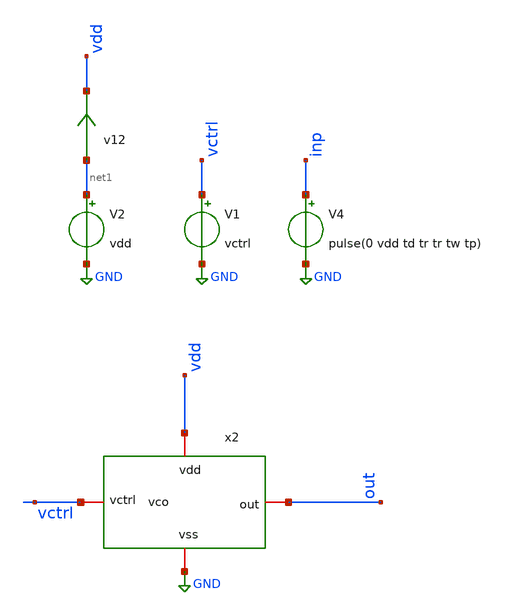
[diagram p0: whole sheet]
** sch_path: xschem/vco/vco_tran.sch
**.subckt vco_tran
V1 vctrl GND vctrl
V2 net1 GND vdd
V4 inp GND pulse(0 vdd td tr tr tw tp)
v12 net1 vdd 0
.save i(v12)
x2 vdd out vctrl GND vco
**** begin user architecture code

** opencircuitdesign pdks install
.lib $::SKYWATER_MODELS/sky130.lib.spice tt
.include $::SKYWATER_STDCELLS/sky130_fd_sc_hd.spice




.options acct list
.temp 25
.save all
.save @m.x2.xm1.msky130_fd_pr__nfet_01v8[cgd]
.save @m.x2.xm4.msky130_fd_pr__pfet_01v8[cgd]
.save @m.x2.xm4.msky130_fd_pr__pfet_01v8[cgg]

.save @m.x2.xm6.msky130_fd_pr__nfet_01v8[cgd]
.save @m.x2.xm6.msky130_fd_pr__nfet_01v8[cgg]

.save @m.x2.xm1.msky130_fd_pr__nfet_01v8[gm]

.save @m.x2.xm2.msky130_fd_pr__pfet_01v8[vth]
.save @m.x2.xm1.msky130_fd_pr__nfet_01v8[vth]
.save @m.x2.xm5.msky130_fd_pr__nfet_01v8[vth]


.param vctrl=0.75 vdd=1.7 cload=250f  td=20n tr=0.1n tw=10n  tp=20n

.control
op
write vco_tran.raw
set appendwrite

tran 0.01n 800n uic
meas tran tdelay01 TRIG v(out) VAL=0.9 RISE=6 TARG v(out) VAL=0.9 RISE=7
let fosc1= 1/tdelay01
print fosc1
save fosc1
remzerovec
write vco_tran.raw
set appendwrite


alterparam vctrl=0.85
reset
tran 0.01n 800n uic
meas tran tdelay01 TRIG v(out) VAL=0.9 RISE=6 TARG v(out) VAL=0.9 RISE=7
let fosc1= 1/tdelay01
print fosc1
save fosc1
remzerovec
write vco_tran.raw
set appendwrite


alterparam vctrl=0.95
reset
tran 0.01n 800n uic
meas tran tdelay01 TRIG v(out) VAL=0.9 RISE=6 TARG v(out) VAL=0.9 RISE=7
let fosc1= 1/tdelay01
print fosc1
save fosc1
remzerovec
write vco_tran.raw
set appendwrite

alterparam vctrl=1.05
reset
tran 0.01n 800n uic
meas tran tdelay01 TRIG v(out) VAL=0.9 RISE=6 TARG v(out) VAL=0.9 RISE=7
let fosc1= 1/tdelay01
print fosc1
save fosc1
remzerovec
write vco_tran.raw
set appendwrite

alterparam vctrl=1.15
reset
tran 0.01n 800n uic
meas tran tdelay01 TRIG v(out) VAL=0.9 RISE=6 TARG v(out) VAL=0.9 RISE=7
let fosc1= 1/tdelay01
print fosc1
save fosc1
remzerovec
write vco_tran.raw
set appendwrite

alterparam vctrl=1.25
reset
tran 0.01n 800n uic
meas tran tdelay01 TRIG v(out) VAL=0.9 RISE=6 TARG v(out) VAL=0.9 RISE=7
let fosc1= 1/tdelay01
print fosc1
save fosc1
remzerovec
write vco_tran.raw
set appendwrite

.endc


**** end user architecture code
**.ends

* expanding   symbol:  vco/vco.sym # of pins=4
** sym_path: xschem01/vco/vco.sym
** sch_path: xschem01/vco/vco.sch
.subckt vco vdd out vctrl vss
*.iopin vdd
*.iopin vss
*.iopin out
*.iopin vctrl
XM1 net1 vctrl vss vss sky130_fd_pr__nfet_01v8 L=0.15 W=30 nf=1 ad='int((nf+1)/2) * W/nf * 0.29' as='int((nf+2)/2) * W/nf * 0.29'
+ pd='2*int((nf+1)/2) * (W/nf + 0.29)' ps='2*int((nf+2)/2) * (W/nf + 0.29)' nrd='0.29 / W' nrs='0.29 / W'
+ sa=0 sb=0 sd=0 mult=1 m=1
XM2 net1 net1 vdd vdd sky130_fd_pr__pfet_01v8 L=0.15 W=90 nf=1 ad='int((nf+1)/2) * W/nf * 0.29' as='int((nf+2)/2) * W/nf * 0.29'
+ pd='2*int((nf+1)/2) * (W/nf + 0.29)' ps='2*int((nf+2)/2) * (W/nf + 0.29)' nrd='0.29 / W' nrs='0.29 / W'
+ sa=0 sb=0 sd=0 mult=1 m=1
XM3 net4 net1 vdd vdd sky130_fd_pr__pfet_01v8 L=0.15 W=80 nf=1 ad='int((nf+1)/2) * W/nf * 0.29' as='int((nf+2)/2) * W/nf * 0.29'
+ pd='2*int((nf+1)/2) * (W/nf + 0.29)' ps='2*int((nf+2)/2) * (W/nf + 0.29)' nrd='0.29 / W' nrs='0.29 / W'
+ sa=0 sb=0 sd=0 mult=1 m=1
XM4 net3 out net4 net4 sky130_fd_pr__pfet_01v8 L=0.15 W=80 nf=1 ad='int((nf+1)/2) * W/nf * 0.29' as='int((nf+2)/2) * W/nf * 0.29'
+ pd='2*int((nf+1)/2) * (W/nf + 0.29)' ps='2*int((nf+2)/2) * (W/nf + 0.29)' nrd='0.29 / W' nrs='0.29 / W'
+ sa=0 sb=0 sd=0 mult=1 m=1
XM5 net2 vctrl vss vss sky130_fd_pr__nfet_01v8 L=0.15 W=30 nf=1 ad='int((nf+1)/2) * W/nf * 0.29' as='int((nf+2)/2) * W/nf * 0.29'
+ pd='2*int((nf+1)/2) * (W/nf + 0.29)' ps='2*int((nf+2)/2) * (W/nf + 0.29)' nrd='0.29 / W' nrs='0.29 / W'
+ sa=0 sb=0 sd=0 mult=1 m=1
XM6 net3 out net2 vss sky130_fd_pr__nfet_01v8 L=0.15 W=30 nf=1 ad='int((nf+1)/2) * W/nf * 0.29' as='int((nf+2)/2) * W/nf * 0.29'
+ pd='2*int((nf+1)/2) * (W/nf + 0.29)' ps='2*int((nf+2)/2) * (W/nf + 0.29)' nrd='0.29 / W' nrs='0.29 / W'
+ sa=0 sb=0 sd=0 mult=1 m=1
XM7 net7 net1 vdd vdd sky130_fd_pr__pfet_01v8 L=0.15 W=80 nf=1 ad='int((nf+1)/2) * W/nf * 0.29' as='int((nf+2)/2) * W/nf * 0.29'
+ pd='2*int((nf+1)/2) * (W/nf + 0.29)' ps='2*int((nf+2)/2) * (W/nf + 0.29)' nrd='0.29 / W' nrs='0.29 / W'
+ sa=0 sb=0 sd=0 mult=2 m=2
XM8 net6 net3 net7 net7 sky130_fd_pr__pfet_01v8 L=0.15 W=80 nf=1 ad='int((nf+1)/2) * W/nf * 0.29' as='int((nf+2)/2) * W/nf * 0.29'
+ pd='2*int((nf+1)/2) * (W/nf + 0.29)' ps='2*int((nf+2)/2) * (W/nf + 0.29)' nrd='0.29 / W' nrs='0.29 / W'
+ sa=0 sb=0 sd=0 mult=2 m=2
XM9 net5 vctrl vss vss sky130_fd_pr__nfet_01v8 L=0.15 W=60 nf=1 ad='int((nf+1)/2) * W/nf * 0.29' as='int((nf+2)/2) * W/nf * 0.29'
+ pd='2*int((nf+1)/2) * (W/nf + 0.29)' ps='2*int((nf+2)/2) * (W/nf + 0.29)' nrd='0.29 / W' nrs='0.29 / W'
+ sa=0 sb=0 sd=0 mult=1 m=1
XM10 net6 net3 net5 vss sky130_fd_pr__nfet_01v8 L=0.15 W=60 nf=1 ad='int((nf+1)/2) * W/nf * 0.29' as='int((nf+2)/2) * W/nf * 0.29'
+ pd='2*int((nf+1)/2) * (W/nf + 0.29)' ps='2*int((nf+2)/2) * (W/nf + 0.29)' nrd='0.29 / W' nrs='0.29 / W'
+ sa=0 sb=0 sd=0 mult=1 m=1
XM11 net9 net1 vdd vdd sky130_fd_pr__pfet_01v8 L=0.15 W=80 nf=1 ad='int((nf+1)/2) * W/nf * 0.29' as='int((nf+2)/2) * W/nf * 0.29'
+ pd='2*int((nf+1)/2) * (W/nf + 0.29)' ps='2*int((nf+2)/2) * (W/nf + 0.29)' nrd='0.29 / W' nrs='0.29 / W'
+ sa=0 sb=0 sd=0 mult=3 m=3
XM12 out net6 net9 net9 sky130_fd_pr__pfet_01v8 L=0.15 W=80 nf=1 ad='int((nf+1)/2) * W/nf * 0.29' as='int((nf+2)/2) * W/nf * 0.29'
+ pd='2*int((nf+1)/2) * (W/nf + 0.29)' ps='2*int((nf+2)/2) * (W/nf + 0.29)' nrd='0.29 / W' nrs='0.29 / W'
+ sa=0 sb=0 sd=0 mult=3 m=3
XM13 net8 vctrl vss vss sky130_fd_pr__nfet_01v8 L=0.15 W=90 nf=1 ad='int((nf+1)/2) * W/nf * 0.29' as='int((nf+2)/2) * W/nf * 0.29'
+ pd='2*int((nf+1)/2) * (W/nf + 0.29)' ps='2*int((nf+2)/2) * (W/nf + 0.29)' nrd='0.29 / W' nrs='0.29 / W'
+ sa=0 sb=0 sd=0 mult=1 m=1
XM14 out net6 net8 vss sky130_fd_pr__nfet_01v8 L=0.15 W=90 nf=1 ad='int((nf+1)/2) * W/nf * 0.29' as='int((nf+2)/2) * W/nf * 0.29'
+ pd='2*int((nf+1)/2) * (W/nf + 0.29)' ps='2*int((nf+2)/2) * (W/nf + 0.29)' nrd='0.29 / W' nrs='0.29 / W'
+ sa=0 sb=0 sd=0 mult=1 m=1
.ends

.GLOBAL GND
.end
